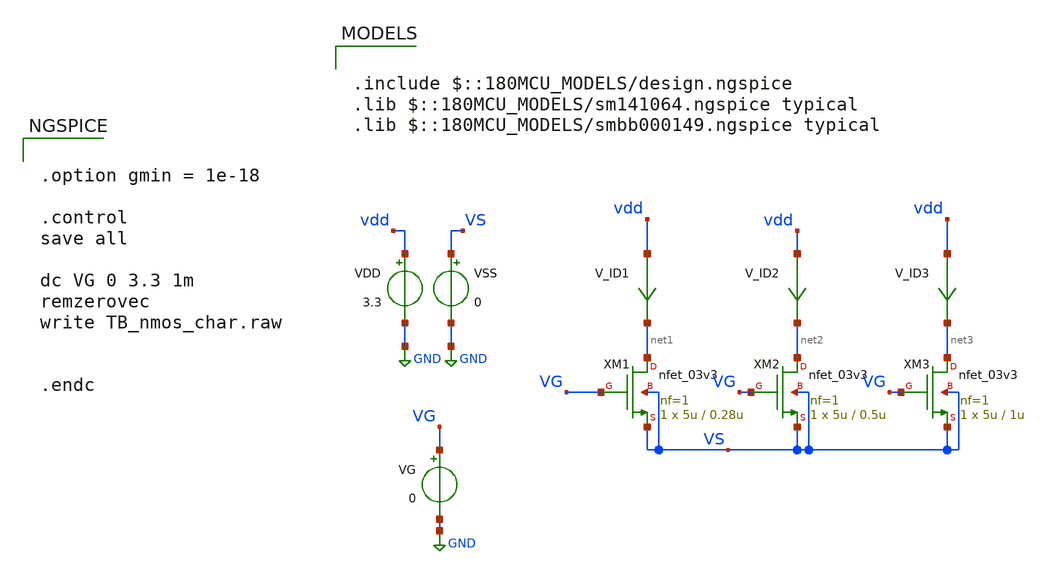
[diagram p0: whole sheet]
** sch_path: Current_Source/TB_nmos_char.sch
**.subckt TB_nmos_char
XM1 net1 VG VS VS nfet_03v3 L=0.28u W=5u nf=1 ad='int((nf+1)/2) * W/nf * 0.18u' as='int((nf+2)/2) * W/nf * 0.18u'
+ pd='2*int((nf+1)/2) * (W/nf + 0.18u)' ps='2*int((nf+2)/2) * (W/nf + 0.18u)' nrd='0.18u / W' nrs='0.18u / W'
+ sa=0 sb=0 sd=0 m=1
XM2 net2 VG VS VS nfet_03v3 L=0.5u W=5u nf=1 ad='int((nf+1)/2) * W/nf * 0.18u' as='int((nf+2)/2) * W/nf * 0.18u'
+ pd='2*int((nf+1)/2) * (W/nf + 0.18u)' ps='2*int((nf+2)/2) * (W/nf + 0.18u)' nrd='0.18u / W' nrs='0.18u / W'
+ sa=0 sb=0 sd=0 m=1
XM3 net3 VG VS VS nfet_03v3 L=1u W=5u nf=1 ad='int((nf+1)/2) * W/nf * 0.18u' as='int((nf+2)/2) * W/nf * 0.18u'
+ pd='2*int((nf+1)/2) * (W/nf + 0.18u)' ps='2*int((nf+2)/2) * (W/nf + 0.18u)' nrd='0.18u / W' nrs='0.18u / W'
+ sa=0 sb=0 sd=0 m=1
V_ID1 vdd net1 0
.save i(v_id1)
V_ID2 vdd net2 0
.save i(v_id2)
V_ID3 vdd net3 0
.save i(v_id3)
VDD vdd GND 3.3
VSS VS GND 0
VG VG GND 0
**** begin user architecture code

.include $::180MCU_MODELS/design.ngspice
.lib $::180MCU_MODELS/sm141064.ngspice typical
.lib $::180MCU_MODELS/smbb000149.ngspice typical



.option gmin = 1e-18

.control
save all

dc VG 0 3.3 1m
remzerovec
write TB_nmos_char.raw


.endc


**** end user architecture code
**.ends
.GLOBAL GND
.end
